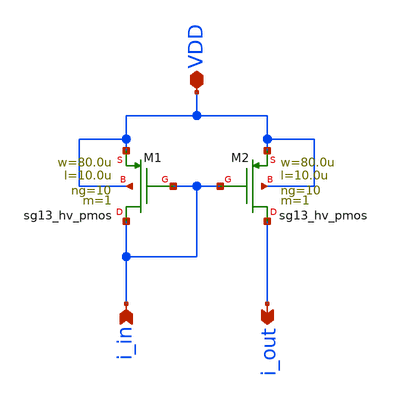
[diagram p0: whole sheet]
** sch_path: macros/heichips26_vcr/macros/switched_capacitor/schematic/xschem/pmos_current_mirror1.sch
**.subckt pmos_current_mirror1 i_in i_out VDD
*.ipin i_in
*.opin i_out
*.iopin VDD
XM2 i_out i_in VDD VDD sg13_hv_pmos w=80.0u l=10.0u ng=10 m=1 mm_ok=1
XM1 i_in i_in VDD VDD sg13_hv_pmos w=80.0u l=10.0u ng=10 m=1 mm_ok=1
**.ends
.end
